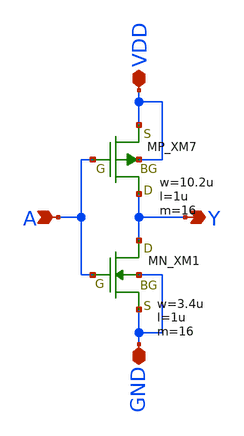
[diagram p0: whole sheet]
** sch_path: openIP62_rev1.0/IP62/Technology/tech/symbols/Xschem/IP62_5_stdcell/INV_X16.sch
**.subckt INV_X16 A Y GND VDD
*.ipin A
*.opin Y
*.iopin GND
*.iopin VDD
XM7 Y A VDD VDD PMOS w=10.2u l=1u as=0 ad=0 ps=0 pd=0 nrd=0 nrs=0 m=16
XM1 Y A GND GND NMOS w=3.4u l=1u as=0 ad=0 ps=0 pd=0 nrd=0 nrs=0 m=16
**.ends
.end
